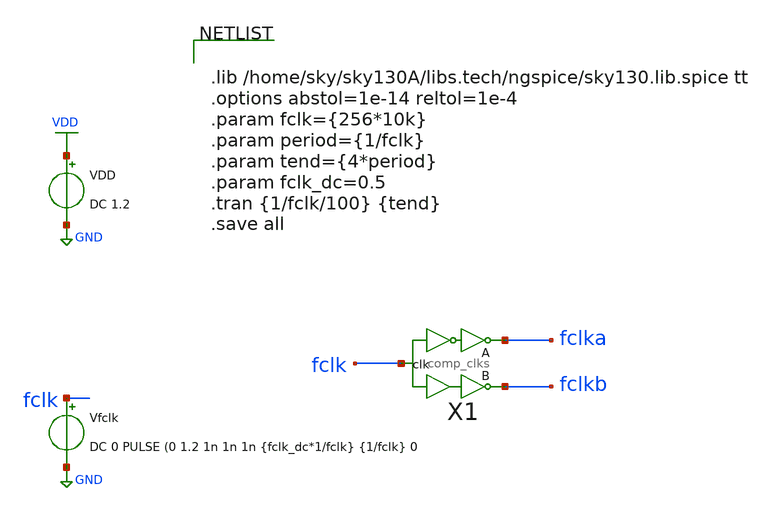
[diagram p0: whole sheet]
** sch_path: xschem/clkgen/comp_clks_tb.sch
**.subckt comp_clks_tb
VDD VDD GND DC 1.2
Vfclk fclk GND DC 0 PULSE (0 1.2 1n 1n 1n {fclk_dc*1/fclk} {1/fclk} 0
X1 fclk fclka fclkb comp_clks Wpmos=3 Lpmos=0.18 Wnmos=1 Lnmos=0.18
**** begin user architecture code


.lib /home/sky/sky130A/libs.tech/ngspice/sky130.lib.spice tt
.options abstol=1e-14 reltol=1e-4
.param fclk={256*10k}
.param period={1/fclk}
.param tend={4*period}
.param fclk_dc=0.5
.tran {1/fclk/100} {tend}
.save all


**** end user architecture code
**.ends
.GLOBAL VDD
.GLOBAL GND
.end
